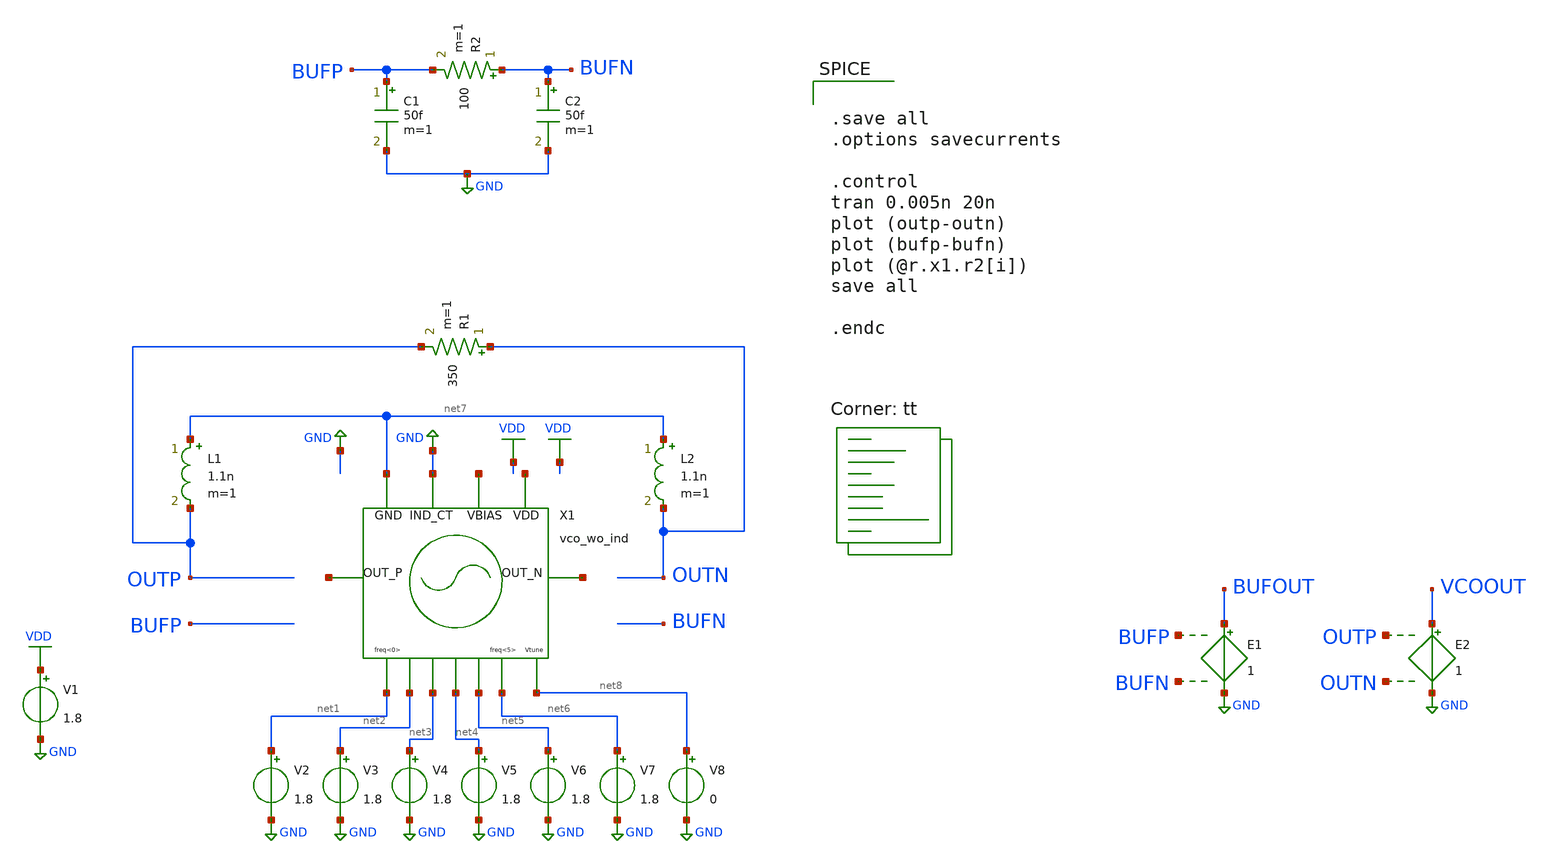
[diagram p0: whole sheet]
** sch_path: xschem/vco_wo_ind_tb.sch
**.subckt vco_wo_ind_tb
V1 VDD GND 1.8
V2 net1 GND 1.8
V3 net2 GND 1.8
V4 net3 GND 1.8
V5 net4 GND 1.8
V6 net5 GND 1.8
V7 net6 GND 1.8
L1 net7 OUTP 1.1n m=1
L2 net7 OUTN 1.1n m=1
V8 net8 GND 0
R1 OUTN OUTP 350 m=1
R2 BUFN BUFP 100 m=1
C1 BUFP GND 50f m=1
C2 BUFN GND 50f m=1
E1 BUFOUT GND BUFP BUFN 1
E2 VCOOUT GND OUTP OUTN 1
X1 net9 net7 GND net10 net11 net1 net2 net3 net4 net5 net6 net12 net8 vco_wo_ind
**** begin user architecture code


.save all
.options savecurrents

.control
tran 0.005n 20n
plot (outp-outn)
plot (bufp-bufn)
plot (@r.x1.r2[i])
save all

.endc


.lib $::SKYWATER_MODELS/sky130.lib.spice tt
**** end user architecture code
**.ends
.GLOBAL GND
.GLOBAL VDD
.end
